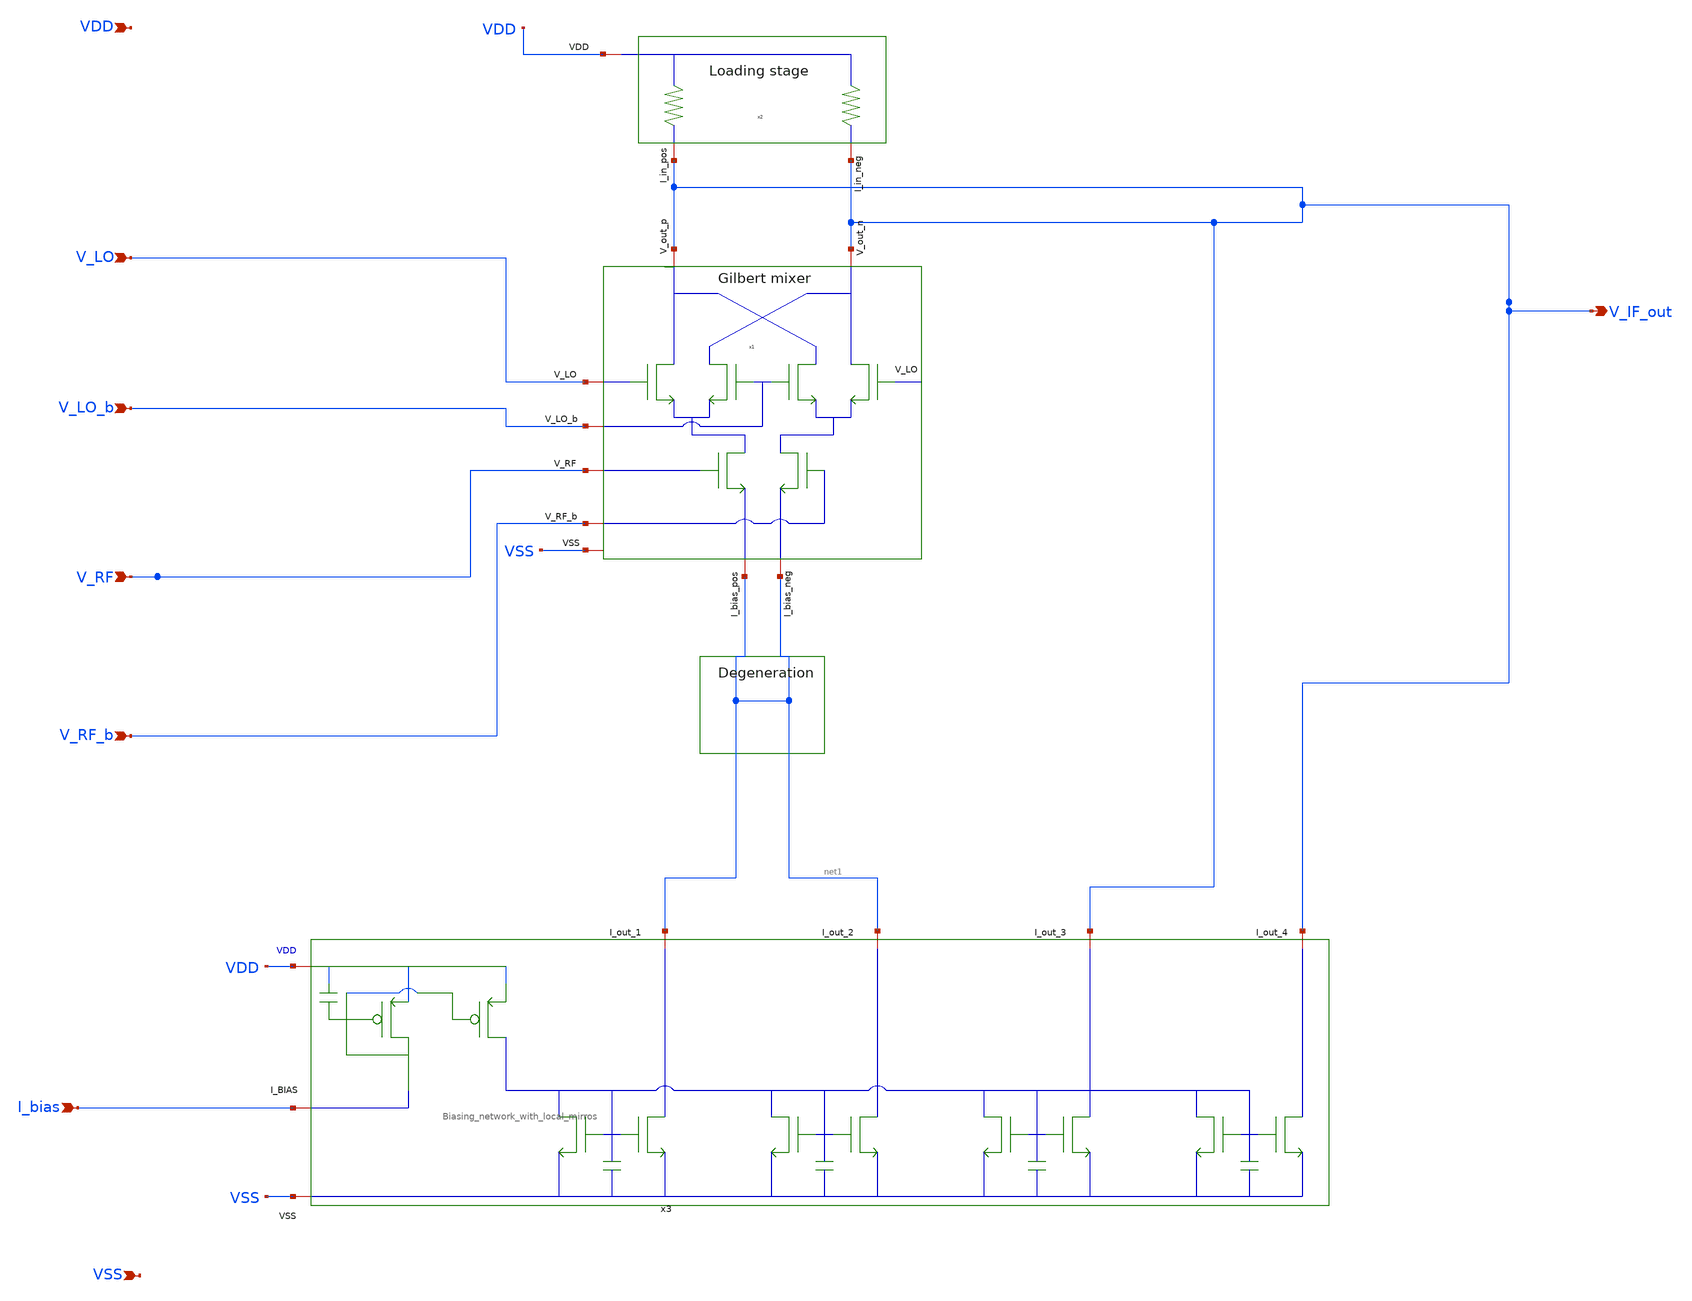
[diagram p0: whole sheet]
** sch_path: src/design_padring/A5_Time_Transcenders_padring_integrated/schematic/Gilbert_mixer_schematic.sch
**.subckt Gilbert_mixer_schematic V_LO V_LO_b V_RF V_RF_b V_IF_out I_bias VSS VDD
*.ipin V_LO
*.ipin V_LO_b
*.ipin V_RF
*.ipin V_RF_b
*.opin V_IF_out
*.ipin I_bias
*.ipin VSS
*.ipin VDD
x1 V_IF_out V_IF_out V_LO V_LO_b V_RF V_RF_b net1 net1 VSS Gilbert_cell_hierarchal_mixing_stage
x2 V_IF_out V_IF_out VDD Gilbert_cell_hierarchal_loading_stage
x3 VDD net1 net1 V_IF_out I_bias VSS V_IF_out Biasing_network_with_local_mirros pmos_l_ref=0.4u
+ pmos_w_ref=2u pmos_l_mir=0.4u pmos_w_mir=8u nmos_l_ref_1=1u nmos_w_ref_1=1.5u nmos_nf_ref_1=1 nmos_l_mir_1=1u
+ nmos_w_mir_1=7.5u nmos_nf_mir_1=5 nmos_l_ref_2=1u nmos_w_ref_2=1.5u nmos_nf_ref_2=1 nmos_l_mir_2=1u nmos_w_mir_2=7.5u
+ nmos_nf_mir_2=5 nmos_l_ref_3=1u nmos_w_ref_3=1.5u nmos_nf_ref_3=2 nmos_l_mir_3=1u nmos_w_mir_3=1.5u nmos_nf_mir_3=2
+ nmos_l_ref_4=1u nmos_w_ref_4=1.5u nmos_nf_ref_4=1 nmos_l_mir_4=1u nmos_w_mir_4=15u nmos_nf_mir_4=10
**.ends
.end
